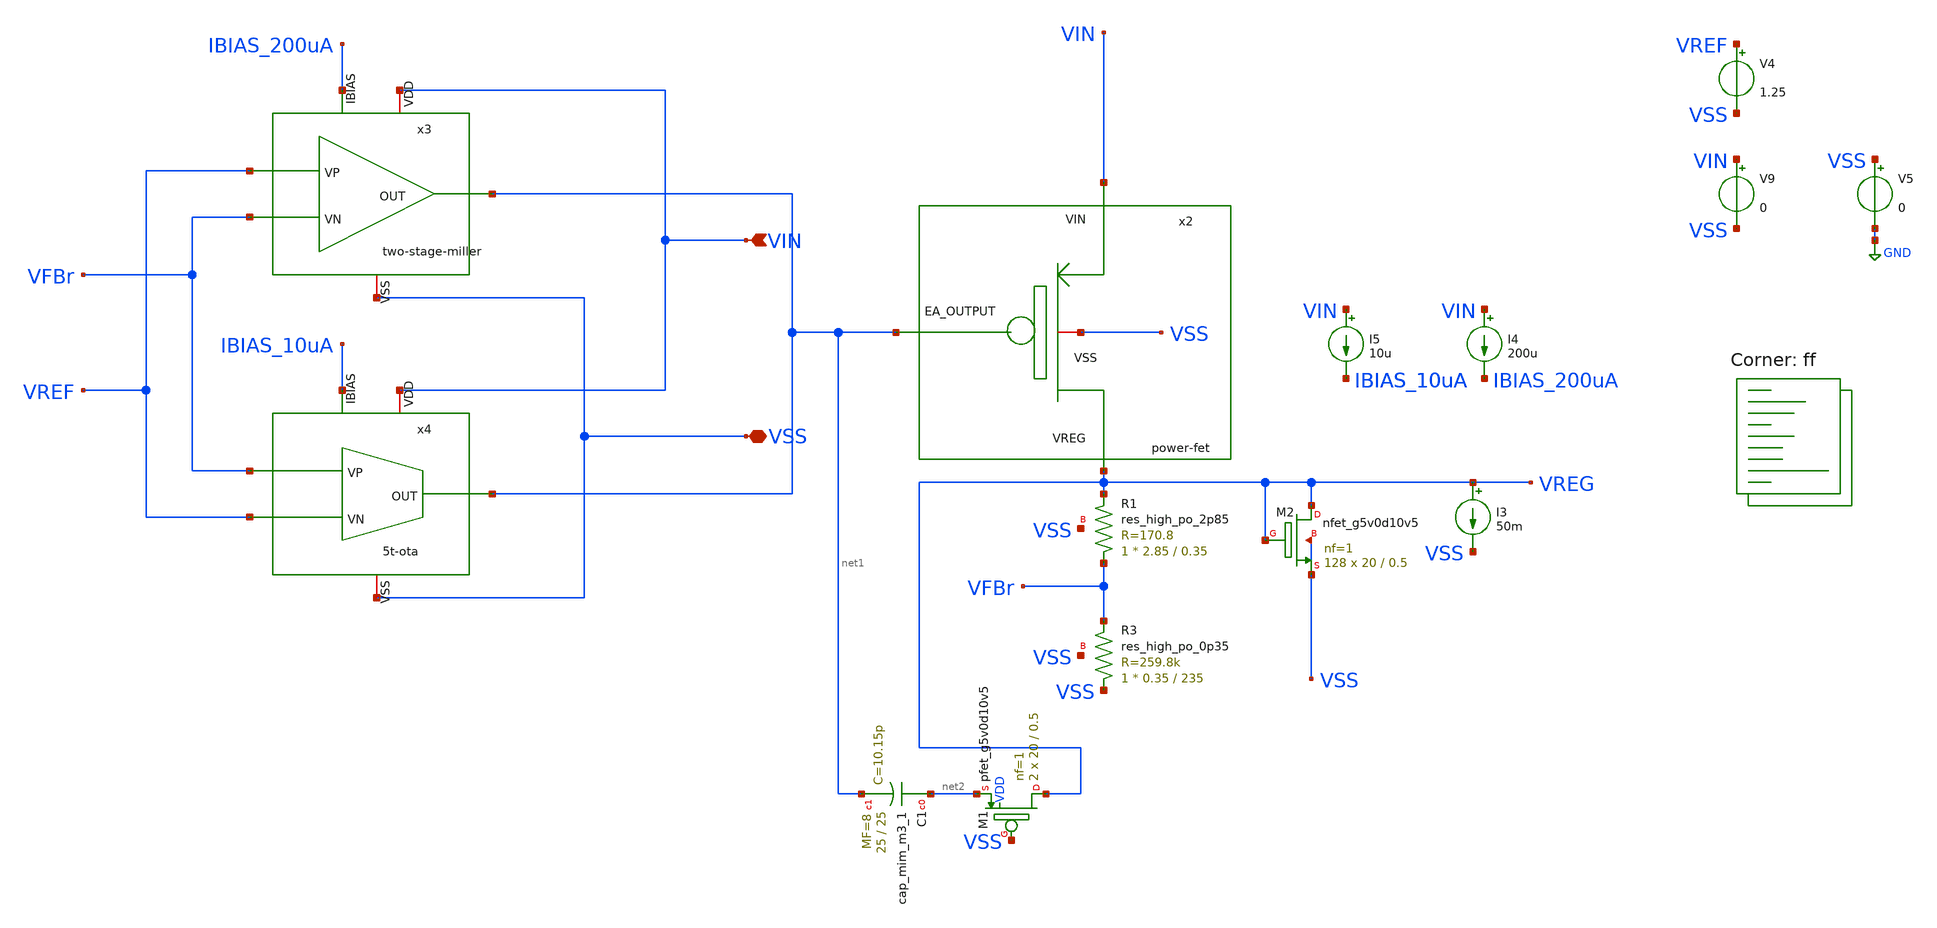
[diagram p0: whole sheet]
** sch_path: bandgap/testbench/tb_dc_load-line.sch
**.subckt tb_dc_load-line VIN VSS
*.ipin VIN
*.iopin VSS
x2 VIN VSS net1 VREG power-fet
XR3 VSS VFBr VSS sky130_fd_pr__res_high_po_0p35 L=235 mult=1 m=1
XR1 VFBr VREG VSS sky130_fd_pr__res_high_po_2p85 L=0.35 mult=1 m=1
x3 VIN net1 VREF VFBr IBIAS_200uA VSS two-stage-miller
x4 VIN net1 IBIAS_10uA VREF VFBr VSS 5t-ota
I4 VIN IBIAS_200uA 200u
I3 VREG VSS 50m
V4 VREF VSS 1.25
V5 VSS GND 0
V9 VIN VSS 0
I5 VIN IBIAS_10uA 10u
XM2 VREG VREG VSS VSS sky130_fd_pr__nfet_g5v0d10v5 L=0.5 W=20 nf=1 ad='int((nf+1)/2) * W/nf * 0.29' as='int((nf+2)/2) * W/nf * 0.29'
+ pd='2*int((nf+1)/2) * (W/nf + 0.29)' ps='2*int((nf+2)/2) * (W/nf + 0.29)' nrd='0.29 / W' nrs='0.29 / W'
+ sa=0 sb=0 sd=0 mult=128 m=128
XC1 net2 net1 sky130_fd_pr__cap_mim_m3_1 W=25 L=25 MF=8 m=8
XM1 VREG VSS net2 VDD sky130_fd_pr__pfet_g5v0d10v5 L=0.5 W=20 nf=1 ad='int((nf+1)/2) * W/nf * 0.29' as='int((nf+2)/2) * W/nf * 0.29'
+ pd='2*int((nf+1)/2) * (W/nf + 0.29)' ps='2*int((nf+2)/2) * (W/nf + 0.29)' nrd='0.29 / W' nrs='0.29 / W'
+ sa=0 sb=0 sd=0 mult=2 m=2
**** begin user architecture code


.control
    * Run the nested sweep
    * V9 (outer): 1.6 to 5.0 (35 steps)
    * I3 (inner): 0 to 50m (100 steps)
    dc V9 1.6 10.0 0.1 I3 0 50m 0.5m

    * In a nested sweep, the total number of points is (OuterSteps * InnerSteps)
    * Inner sweep has (50m - 0) / 0.5m + 1 = 101 points.

    * 1. LINE REGULATION
    * We want VREG at Iload=0 for Vin=5.0 and Vin=1.6
    * Point at Vin=1.6, I3=0 is index [0]
    * Point at Vin=5.0, I3=0 is index [34 * 101]
    let vreg_low = v(VREG)[0]
    let vreg_high = v(VREG)[3434]
    let line_reg = (vreg_high - vreg_low) / (5.0 - 1.6)

    * 2. LOAD REGULATION
    * We calculate this at a fixed Vin (e.g., the last sweep at Vin=5.0)
    * Full load (50mA) is the last point of that sweep
    let vreg_no_load = v(VREG)[3434]
    let vreg_full_load = v(VREG)[3534]
    let load_reg = (vreg_no_load - vreg_full_load) / 50m

    * 3. VOLTAGE DRIFT
    * Use vecmax and vecmin for vectors
    let v_max = vecmax(v(VREG))
    let v_min = vecmin(v(VREG))
    let v_drift = v_max - v_min

    * Print Results
    echo ==== REGULATION ANALYSIS ====
    print line_reg
    print load_reg
    print v_drift
    echo =============================

    plot v(VREG)
.endc


.lib $::SKYWATER_MODELS/sky130.lib.spice ff
**** end user architecture code
**.ends
.GLOBAL GND
.end
